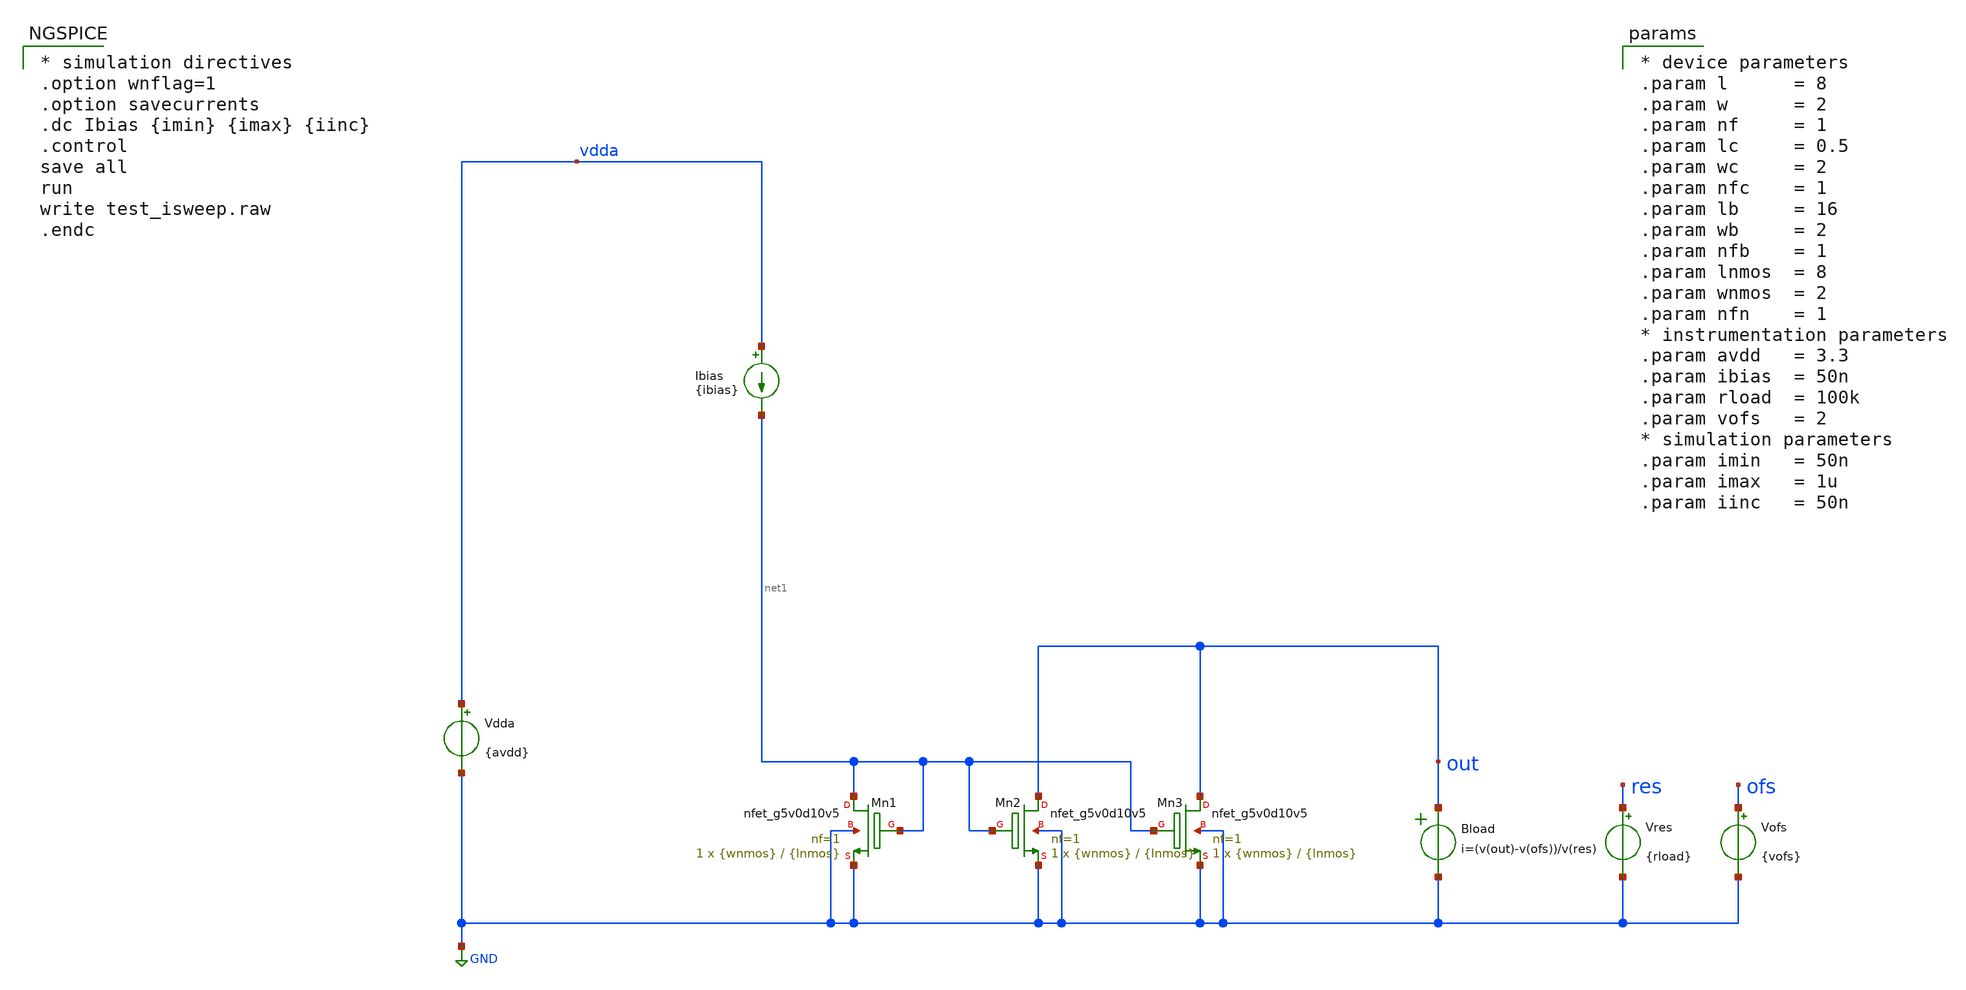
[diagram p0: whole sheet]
** sch_path: xschem/test_isweep.sch
**.subckt test_isweep
Vdda vdda GND {avdd}
.save i(vdda)
Ibias vdda net1 {ibias}
Vres res GND {rload}
Bload out GND i=(v(out)-v(ofs))/v(res)
Vofs ofs GND {vofs}
XMn1 net1 net1 GND GND sky130_fd_pr__nfet_g5v0d10v5 L={lnmos} W={wnmos} nf=1 ad='int((1 + 1)/2) * {wnmos} / 1 * 0.29'
+ as='int((1 + 2)/2) * {wnmos} / 1 * 0.29' pd='2*int((1 + 1)/2) * ({wnmos} / 1 + 0.29)' ps='2*int((1 + 2)/2) * ({wnmos} / 1 + 0.29)'
+ nrd='0.29 / {wnmos} ' nrs='0.29 / {wnmos} ' sa=0 sb=0 sd=0 mult=1 m=1
XMn2 out net1 GND GND sky130_fd_pr__nfet_g5v0d10v5 L={lnmos} W={wnmos} nf=1 ad='int((1 + 1)/2) * {wnmos} / 1 * 0.29'
+ as='int((1 + 2)/2) * {wnmos} / 1 * 0.29' pd='2*int((1 + 1)/2) * ({wnmos} / 1 + 0.29)' ps='2*int((1 + 2)/2) * ({wnmos} / 1 + 0.29)'
+ nrd='0.29 / {wnmos} ' nrs='0.29 / {wnmos} ' sa=0 sb=0 sd=0 mult=1 m=1
XMn3 out net1 GND GND sky130_fd_pr__nfet_g5v0d10v5 L={lnmos} W={wnmos} nf=1 ad='int((1 + 1)/2) * {wnmos} / 1 * 0.29'
+ as='int((1 + 2)/2) * {wnmos} / 1 * 0.29' pd='2*int((1 + 1)/2) * ({wnmos} / 1 + 0.29)' ps='2*int((1 + 2)/2) * ({wnmos} / 1 + 0.29)'
+ nrd='0.29 / {wnmos} ' nrs='0.29 / {wnmos} ' sa=0 sb=0 sd=0 mult=1 m=1
**** begin user architecture code

* device parameters
.param l      = 8
.param w      = 2
.param nf     = 1
.param lc     = 0.5
.param wc     = 2
.param nfc    = 1
.param lb     = 16
.param wb     = 2
.param nfb    = 1
.param lnmos  = 8
.param wnmos  = 2
.param nfn    = 1
* instrumentation parameters
.param avdd   = 3.3
.param ibias  = 50n
.param rload  = 100k
.param vofs   = 2
* simulation parameters
.param imin   = 50n
.param imax   = 1u
.param iinc   = 50n


** opencircuitdesign pdks install
.lib $::SKYWATER_MODELS/sky130.lib.spice tt



* simulation directives
.option wnflag=1
.option savecurrents
.dc Ibias {imin} {imax} {iinc}
.control
save all
run
write test_isweep.raw
.endc


**** end user architecture code
**.ends
.GLOBAL GND
.end
